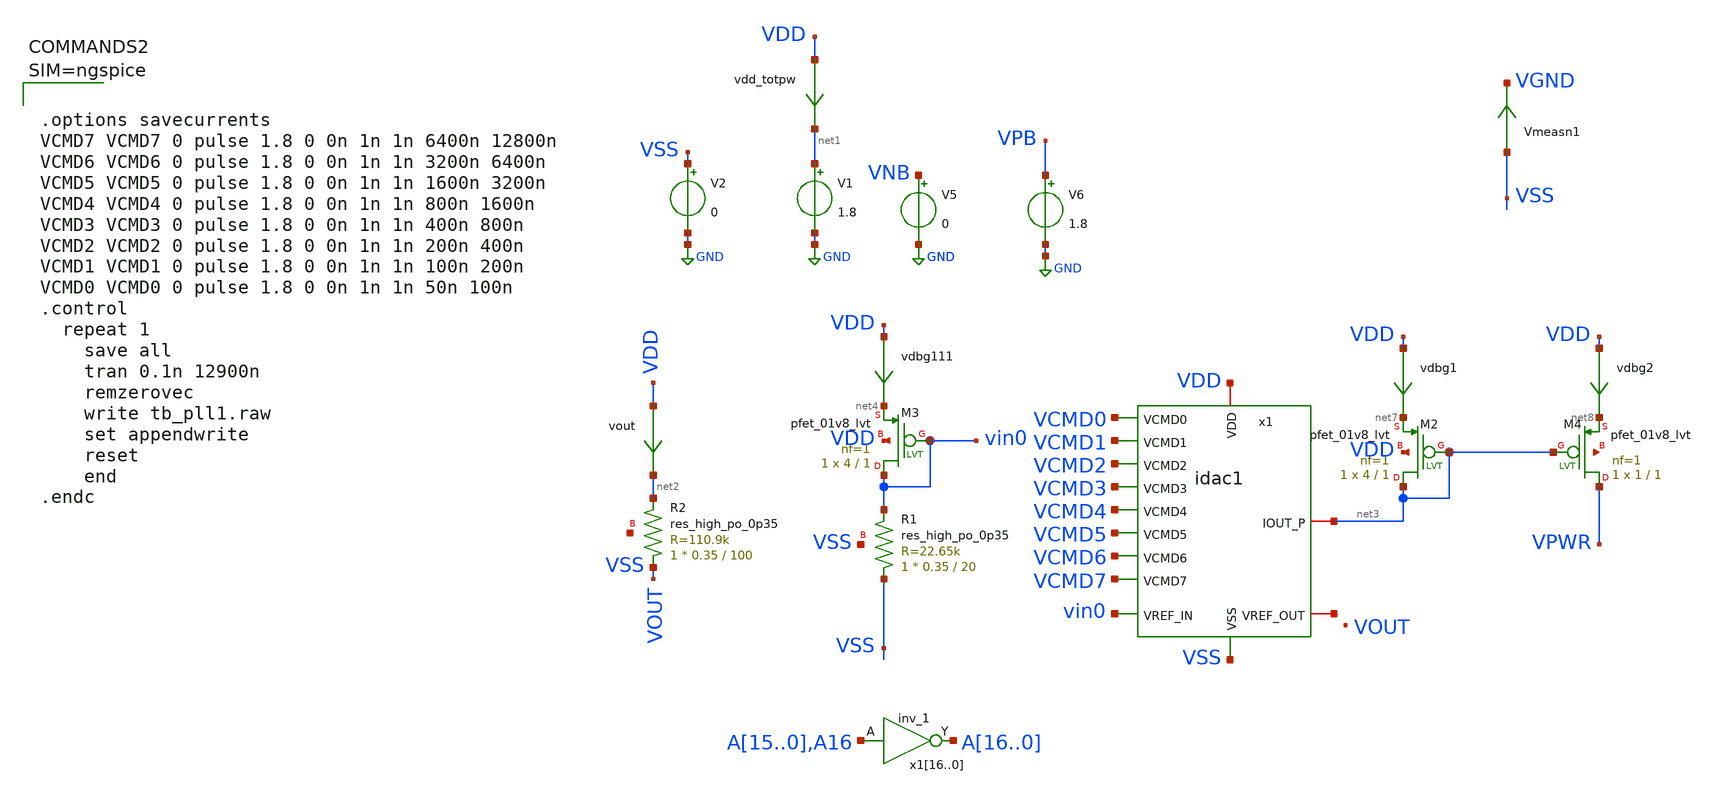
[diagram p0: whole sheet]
** sch_path: tt_um_emilian_rf_playground/xschem/tb_pll1.sch
**.subckt tb_pll1
V5 VNB GND 0
V6 VPB GND 1.8
V1 net1 GND 1.8
V2 VSS GND 0
XM3 vin0 vin0 net4 VDD sky130_fd_pr__pfet_01v8_lvt L=1 W=4 nf=1 ad='int((nf+1)/2) * W/nf * 0.29' as='int((nf+2)/2) * W/nf * 0.29'
+ pd='2*int((nf+1)/2) * (W/nf + 0.29)' ps='2*int((nf+2)/2) * (W/nf + 0.29)' nrd='0.29 / W' nrs='0.29 / W'
+ sa=0 sb=0 sd=0 mult=1 m=1
vout VDD net2 0
.save i(vout)
XR1 VSS vin0 VSS sky130_fd_pr__res_high_po_0p35 L=20 mult=1 m=1
vdbg111 VDD net4 0
.save i(vdbg111)
XR2 VOUT net2 net5 sky130_fd_pr__res_high_po_0p35 L=100 mult=1 m=1
vdd_totpw VDD net1 0
.save i(vdd_totpw)
x1 VCMD0 VCMD1 VCMD2 VCMD3 VCMD4 VCMD5 VCMD6 VCMD7 VDD vin0 VSS net6 net3 idac1
x116 A15 VGND VNB VPB VPWR A16 sky130_fd_sc_hd__inv_1
x115 A14 VGND VNB VPB VPWR A15 sky130_fd_sc_hd__inv_1
x114 A13 VGND VNB VPB VPWR A14 sky130_fd_sc_hd__inv_1
x113 A12 VGND VNB VPB VPWR A13 sky130_fd_sc_hd__inv_1
x112 A11 VGND VNB VPB VPWR A12 sky130_fd_sc_hd__inv_1
x111 A10 VGND VNB VPB VPWR A11 sky130_fd_sc_hd__inv_1
x110 A9 VGND VNB VPB VPWR A10 sky130_fd_sc_hd__inv_1
x19 A8 VGND VNB VPB VPWR A9 sky130_fd_sc_hd__inv_1
x18 A7 VGND VNB VPB VPWR A8 sky130_fd_sc_hd__inv_1
x17 A6 VGND VNB VPB VPWR A7 sky130_fd_sc_hd__inv_1
x16 A5 VGND VNB VPB VPWR A6 sky130_fd_sc_hd__inv_1
x15 A4 VGND VNB VPB VPWR A5 sky130_fd_sc_hd__inv_1
x14 A3 VGND VNB VPB VPWR A4 sky130_fd_sc_hd__inv_1
x13 A2 VGND VNB VPB VPWR A3 sky130_fd_sc_hd__inv_1
x12 A1 VGND VNB VPB VPWR A2 sky130_fd_sc_hd__inv_1
x11 A0 VGND VNB VPB VPWR A1 sky130_fd_sc_hd__inv_1
x10 A16 VGND VNB VPB VPWR A0 sky130_fd_sc_hd__inv_1
Vmeasn1 VSS VGND 0
.save i(vmeasn1)
XM2 net3 net3 net7 VDD sky130_fd_pr__pfet_01v8_lvt L=1 W=4 nf=1 ad='int((nf+1)/2) * W/nf * 0.29' as='int((nf+2)/2) * W/nf * 0.29'
+ pd='2*int((nf+1)/2) * (W/nf + 0.29)' ps='2*int((nf+2)/2) * (W/nf + 0.29)' nrd='0.29 / W' nrs='0.29 / W'
+ sa=0 sb=0 sd=0 mult=1 m=1
vdbg1 VDD net7 0
.save i(vdbg1)
XM4 VPWR net3 net8 net9 sky130_fd_pr__pfet_01v8_lvt L=1 W=1 nf=1 ad='int((nf+1)/2) * W/nf * 0.29' as='int((nf+2)/2) * W/nf * 0.29'
+ pd='2*int((nf+1)/2) * (W/nf + 0.29)' ps='2*int((nf+2)/2) * (W/nf + 0.29)' nrd='0.29 / W' nrs='0.29 / W'
+ sa=0 sb=0 sd=0 mult=1 m=1
vdbg2 VDD net8 0
.save i(vdbg2)
**** begin user architecture code

** opencircuitdesign pdks install
.lib $::SKYWATER_MODELS/sky130.lib.spice tt_mm
*.lib $::SKYWATER_STDCELLS/sky130_fd_sc_hd_blablabla.spice

.subckt sky130_fd_sc_hd__inv_1 A VGND VNB VPB VPWR Y
X0 VGND A Y VNB sky130_fd_pr__nfet_01v8 w=650000u l=150000u
X1 VPWR A Y VPB sky130_fd_pr__pfet_01v8_hvt w=1e+06u l=150000u
.ends





.options savecurrents
VCMD7 VCMD7 0 pulse 1.8 0 0n 1n 1n 6400n 12800n
VCMD6 VCMD6 0 pulse 1.8 0 0n 1n 1n 3200n 6400n
VCMD5 VCMD5 0 pulse 1.8 0 0n 1n 1n 1600n 3200n
VCMD4 VCMD4 0 pulse 1.8 0 0n 1n 1n 800n 1600n
VCMD3 VCMD3 0 pulse 1.8 0 0n 1n 1n 400n 800n
VCMD2 VCMD2 0 pulse 1.8 0 0n 1n 1n 200n 400n
VCMD1 VCMD1 0 pulse 1.8 0 0n 1n 1n 100n 200n
VCMD0 VCMD0 0 pulse 1.8 0 0n 1n 1n 50n 100n
.control
  repeat 1
    save all
    tran 0.1n 12900n
    remzerovec
    write tb_pll1.raw
    set appendwrite
    reset
    end
.endc



**** end user architecture code
**.ends

* expanding   symbol:  idac1.sym # of pins=13
** sym_path: tt_um_emilian_rf_playground/xschem/idac1.sym
** sch_path: tt_um_emilian_rf_playground/xschem/idac1.sch
.subckt idac1 VCMD0 VCMD1 VCMD2 VCMD3 VCMD4 VCMD5 VCMD6 VCMD7 VDD VREF_IN VSS VREF_OUT IOUT_P
*.ipin VSS
*.iopin VREF_IN
*.iopin VDD
*.ipin VCMD7
*.ipin VCMD6
*.ipin VCMD5
*.ipin VCMD4
*.ipin VCMD3
*.ipin VCMD2
*.ipin VCMD1
*.ipin VCMD0
*.iopin VREF_OUT
*.iopin IOUT_P
xcell7 vin6 VREF_OUT IOUT VDD VSS VCMD0 idac1cell
xcell6 vin5 vin6 IOUT VDD VSS VCMD1 idac1cell
xcell5 vin4 vin5 IOUT VDD VSS VCMD2 idac1cell
xcell4 vin3 vin4 IOUT VDD VSS VCMD3 idac1cell
xcell3 vin2 vin3 IOUT VDD VSS VCMD4 idac1cell
xcell2 vin1 vin2 IOUT VDD VSS VCMD5 idac1cell
xcell1 vin0 vin1 IOUT VDD VSS VCMD6 idac1cell
xcell0 VREF_IN vin0 IOUT VDD VSS VCMD7 idac1cell
XM2 IOUT IOUT net1 VDD sky130_fd_pr__pfet_01v8_lvt L=1 W=4 nf=1 ad='int((nf+1)/2) * W/nf * 0.29' as='int((nf+2)/2) * W/nf * 0.29'
+ pd='2*int((nf+1)/2) * (W/nf + 0.29)' ps='2*int((nf+2)/2) * (W/nf + 0.29)' nrd='0.29 / W' nrs='0.29 / W'
+ sa=0 sb=0 sd=0 mult=1 m=1
vdbg1 VDD net1 0
.save i(vdbg1)
XM4 IOUT_P IOUT net2 VDD sky130_fd_pr__pfet_01v8_lvt L=1 W=4 nf=1 ad='int((nf+1)/2) * W/nf * 0.29' as='int((nf+2)/2) * W/nf * 0.29'
+ pd='2*int((nf+1)/2) * (W/nf + 0.29)' ps='2*int((nf+2)/2) * (W/nf + 0.29)' nrd='0.29 / W' nrs='0.29 / W'
+ sa=0 sb=0 sd=0 mult=1 m=1
vdbg2 VDD net2 0
.save i(vdbg2)
.ends


* expanding   symbol:  idac1cell.sym # of pins=6
** sym_path: tt_um_emilian_rf_playground/xschem/idac1cell.sym
** sch_path: tt_um_emilian_rf_playground/xschem/idac1cell.sch
.subckt idac1cell VREF_IN VREF_OUT IOUT VDD VSS OE
*.ipin VSS
*.iopin VREF_OUT
*.ipin VREF_IN
*.iopin VDD
*.iopin IOUT
*.ipin OE
XM3 net1 net1 net2 net2 sky130_fd_pr__nfet_01v8_lvt L=1 W=2 nf=1 ad='int((nf+1)/2) * W/nf * 0.29' as='int((nf+2)/2) * W/nf * 0.29'
+ pd='2*int((nf+1)/2) * (W/nf + 0.29)' ps='2*int((nf+2)/2) * (W/nf + 0.29)' nrd='0.29 / W' nrs='0.29 / W'
+ sa=0 sb=0 sd=0 mult=1 m=1
XM4 net1 net1 VSS VSS sky130_fd_pr__nfet_01v8_lvt L=1 W=2 nf=1 ad='int((nf+1)/2) * W/nf * 0.29' as='int((nf+2)/2) * W/nf * 0.29'
+ pd='2*int((nf+1)/2) * (W/nf + 0.29)' ps='2*int((nf+2)/2) * (W/nf + 0.29)' nrd='0.29 / W' nrs='0.29 / W'
+ sa=0 sb=0 sd=0 mult=1 m=1
XM1 net1 VREF_IN VDD VDD sky130_fd_pr__pfet_01v8_lvt L=1 W=4 nf=1 ad='int((nf+1)/2) * W/nf * 0.29' as='int((nf+2)/2) * W/nf * 0.29'
+ pd='2*int((nf+1)/2) * (W/nf + 0.29)' ps='2*int((nf+2)/2) * (W/nf + 0.29)' nrd='0.29 / W' nrs='0.29 / W'
+ sa=0 sb=0 sd=0 mult=1 m=1
XM5 net3 net1 VSS VSS sky130_fd_pr__nfet_01v8_lvt L=1 W=2 nf=1 ad='int((nf+1)/2) * W/nf * 0.29' as='int((nf+2)/2) * W/nf * 0.29'
+ pd='2*int((nf+1)/2) * (W/nf + 0.29)' ps='2*int((nf+2)/2) * (W/nf + 0.29)' nrd='0.29 / W' nrs='0.29 / W'
+ sa=0 sb=0 sd=0 mult=1 m=1
XM2 VREF_OUT VREF_OUT VDD VDD sky130_fd_pr__pfet_01v8_lvt L=1 W=4 nf=1 ad='int((nf+1)/2) * W/nf * 0.29'
+ as='int((nf+2)/2) * W/nf * 0.29' pd='2*int((nf+1)/2) * (W/nf + 0.29)' ps='2*int((nf+2)/2) * (W/nf + 0.29)'
+ nrd='0.29 / W' nrs='0.29 / W' sa=0 sb=0 sd=0 mult=1 m=1
XM6 vdrain2 net1 VSS VSS sky130_fd_pr__nfet_01v8_lvt L=1 W=2 nf=1 ad='int((nf+1)/2) * W/nf * 0.29' as='int((nf+2)/2) * W/nf * 0.29'
+ pd='2*int((nf+1)/2) * (W/nf + 0.29)' ps='2*int((nf+2)/2) * (W/nf + 0.29)' nrd='0.29 / W' nrs='0.29 / W'
+ sa=0 sb=0 sd=0 mult=1 m=1
XM7 net4 OE vdrain2 VSS sky130_fd_pr__nfet_01v8_lvt L=1 W=2 nf=1 ad='int((nf+1)/2) * W/nf * 0.29' as='int((nf+2)/2) * W/nf * 0.29'
+ pd='2*int((nf+1)/2) * (W/nf + 0.29)' ps='2*int((nf+2)/2) * (W/nf + 0.29)' nrd='0.29 / W' nrs='0.29 / W'
+ sa=0 sb=0 sd=0 mult=1 m=1
vmeas VREF_OUT net3 0
.save i(vmeas)
viout IOUT net4 0
.save i(viout)
vref net2 VSS 0
.save i(vref)
.ends

.GLOBAL GND
.end
